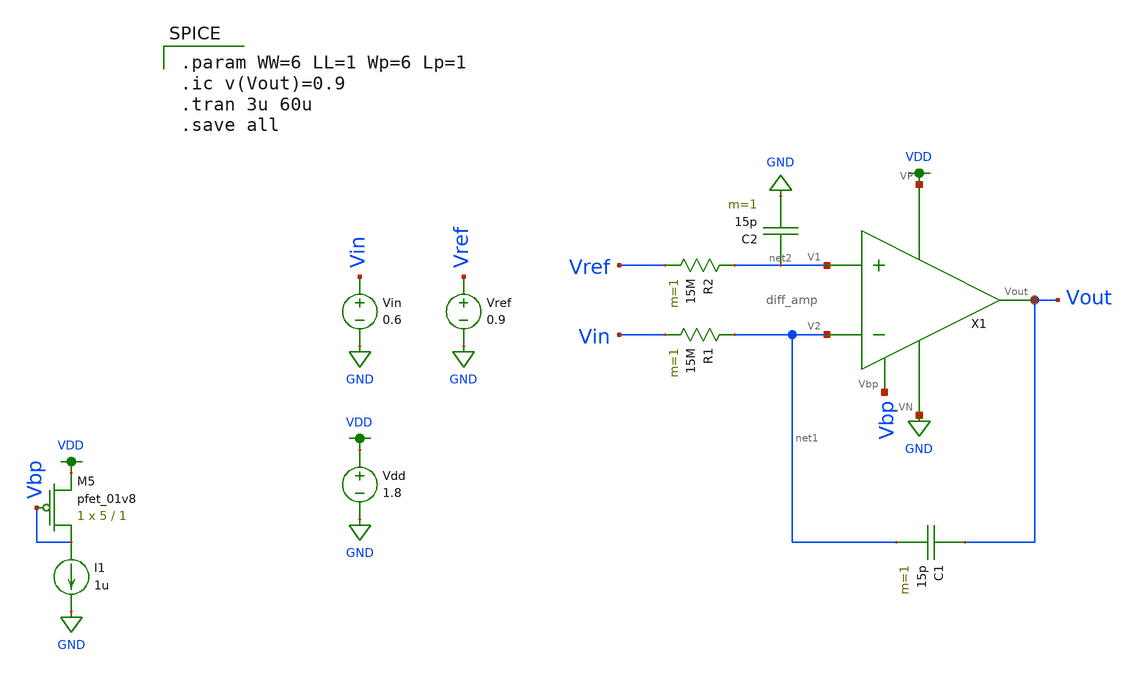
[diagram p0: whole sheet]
** sch_path: schematic/archive/fg_integrator.sch
**.subckt fg_integrator
Vdd VDD GND 1.8
XM5 Vbp Vbp VDD VDD sky130_fd_pr__pfet_01v8 L=1 W=5 nf=1 ad='int((nf+1)/2) * W/nf * 0.29' as='int((nf+2)/2) * W/nf * 0.29'
+ pd='2*int((nf+1)/2) * (W/nf + 0.29)' ps='2*int((nf+2)/2) * (W/nf + 0.29)' nrd='0.29 / W' nrs='0.29 / W'
+ sa=0 sb=0 sd=0 mult=1 m=1
I1 Vbp GND 1u
C1 Vout net1 15p m=1
Vin Vin GND 0.6
X1 VDD Vbp Vout net2 net1 GND diff_amp
R1 net1 Vin 15M m=1
Vref Vref GND 0.9
R2 net2 Vref 15M m=1
C2 net2 GND 15p m=1
**** begin user architecture code

.param WW=6 LL=1 Wp=6 Lp=1
.ic v(Vout)=0.9
.tran 3u 60u
.save all


.option wnflag=1
.param MC_SWITCH=0.0
.lib ~/skywater/skywater-pdk/libraries/sky130_fd_pr_ngspice/latest/models/sky130.lib.spice tt

**** end user architecture code
**.ends
.GLOBAL GND
.GLOBAL VDD
.end
